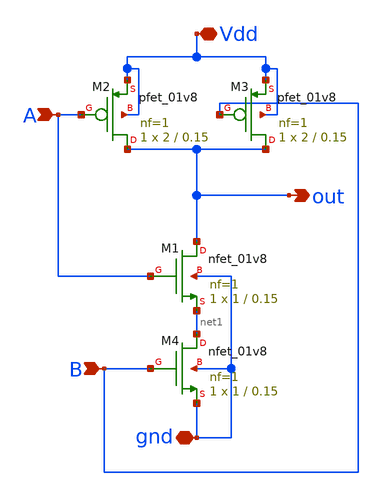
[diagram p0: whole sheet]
** sch_path: Gates/NAND/Schematic/nand.sch
**.subckt nand out Vdd gnd A B
*.opin out
*.iopin Vdd
*.iopin gnd
*.ipin A
*.ipin B
XM1 out A net1 gnd sky130_fd_pr__nfet_01v8 L=0.15 W=1 nf=1 ad='int((nf+1)/2) * W/nf * 0.29' as='int((nf+2)/2) * W/nf * 0.29'
+ pd='2*int((nf+1)/2) * (W/nf + 0.29)' ps='2*int((nf+2)/2) * (W/nf + 0.29)' nrd='0.29 / W' nrs='0.29 / W'
+ sa=0 sb=0 sd=0 mult=1 m=1
XM2 out A Vdd Vdd sky130_fd_pr__pfet_01v8 L=0.15 W=2 nf=1 ad='int((nf+1)/2) * W/nf * 0.29' as='int((nf+2)/2) * W/nf * 0.29'
+ pd='2*int((nf+1)/2) * (W/nf + 0.29)' ps='2*int((nf+2)/2) * (W/nf + 0.29)' nrd='0.29 / W' nrs='0.29 / W'
+ sa=0 sb=0 sd=0 mult=1 m=1
XM3 out B Vdd Vdd sky130_fd_pr__pfet_01v8 L=0.15 W=2 nf=1 ad='int((nf+1)/2) * W/nf * 0.29' as='int((nf+2)/2) * W/nf * 0.29'
+ pd='2*int((nf+1)/2) * (W/nf + 0.29)' ps='2*int((nf+2)/2) * (W/nf + 0.29)' nrd='0.29 / W' nrs='0.29 / W'
+ sa=0 sb=0 sd=0 mult=1 m=1
XM4 net1 B gnd gnd sky130_fd_pr__nfet_01v8 L=0.15 W=1 nf=1 ad='int((nf+1)/2) * W/nf * 0.29' as='int((nf+2)/2) * W/nf * 0.29'
+ pd='2*int((nf+1)/2) * (W/nf + 0.29)' ps='2*int((nf+2)/2) * (W/nf + 0.29)' nrd='0.29 / W' nrs='0.29 / W'
+ sa=0 sb=0 sd=0 mult=1 m=1
**.ends
.end
